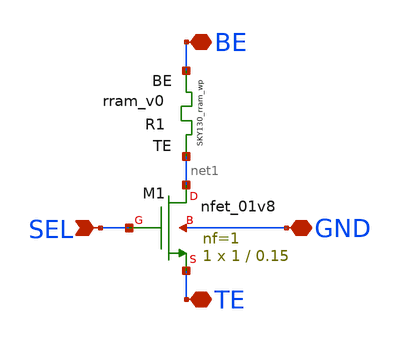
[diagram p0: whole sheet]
** sch_path: Ricardo/1T1R/1T1R.sch
**.subckt 1T1R SEL BE TE GND
*.ipin SEL
*.iopin BE
*.iopin TE
*.iopin GND
XR1 net1 BE rram_v0
XM1 net1 SEL TE GND sky130_fd_pr__nfet_01v8 L=0.15 W=1 nf=1 ad='int((nf+1)/2) * W/nf * 0.29' as='int((nf+2)/2) * W/nf * 0.29'
+ pd='2*int((nf+1)/2) * (W/nf + 0.29)' ps='2*int((nf+2)/2) * (W/nf + 0.29)' nrd='0.29 / W' nrs='0.29 / W'
+ sa=0 sb=0 sd=0 mult=1 m=1
**.ends
.end
